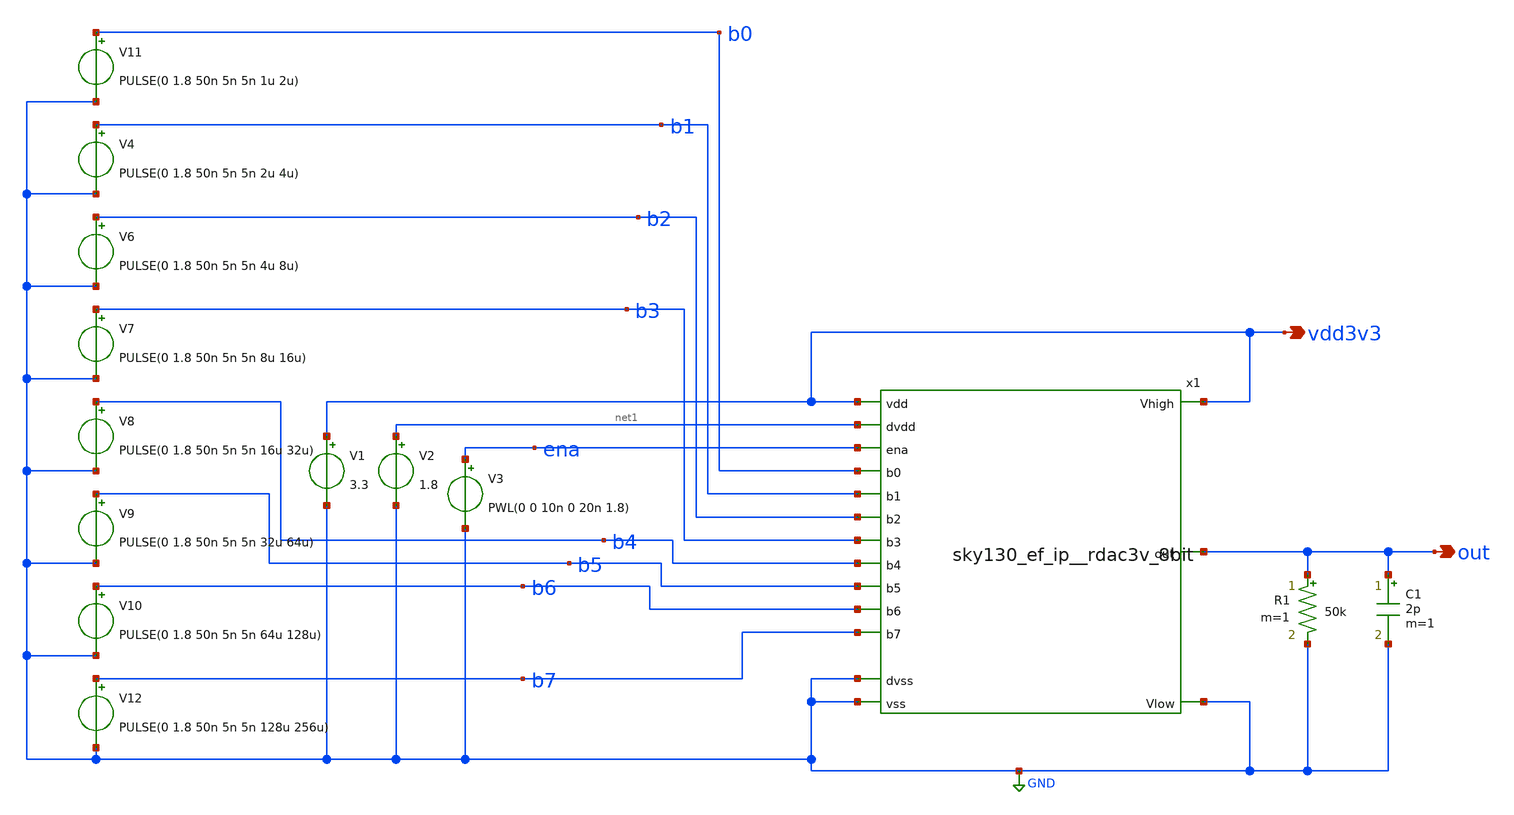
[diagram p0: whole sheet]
** sch_path: xschem/sky130_ef_ip__rdac3v_8bit_tb.sch
**.subckt sky130_ef_ip__rdac3v_8bit_tb out vdd3v3
*.opin out
*.opin vdd3v3
x1 net1 GND GND vdd3v3 b0 vdd3v3 b1 b2 b3 out b4 b5 ena b6 b7 GND sky130_ef_ip__rdac3v_8bit
V1 vdd3v3 GND 3.3
V2 net1 GND 1.8
V3 ena GND PWL(0 0 10n 0 20n 1.8)
V11 b0 GND PULSE(0 1.8 50n 5n 5n 1u 2u)
V4 b1 GND PULSE(0 1.8 50n 5n 5n 2u 4u)
V6 b2 GND PULSE(0 1.8 50n 5n 5n 4u 8u)
V7 b3 GND PULSE(0 1.8 50n 5n 5n 8u 16u)
V8 b4 GND PULSE(0 1.8 50n 5n 5n 16u 32u)
V9 b5 GND PULSE(0 1.8 50n 5n 5n 32u 64u)
V10 b6 GND PULSE(0 1.8 50n 5n 5n 64u 128u)
V12 b7 GND PULSE(0 1.8 50n 5n 5n 128u 256u)
R1 out GND 50k m=1
C1 out GND 2p m=1
**** begin user architecture code


.lib /usr/share/pdk/sky130A/libs.tech/ngspice/sky130.lib.spice tt
.include /usr/share/pdk/sky130A/libs.ref/sky130_fd_sc_hvl/spice/sky130_fd_sc_hvl.spice




.control
tran 50m 256u
plot V(out)
.endc

**** end user architecture code
**.ends
.GLOBAL GND
.end
